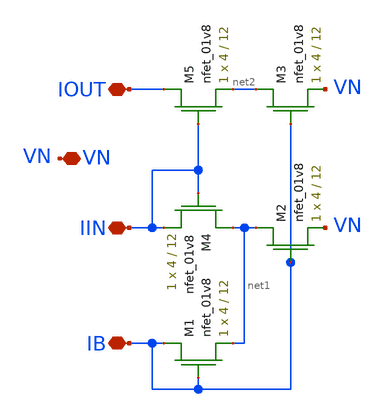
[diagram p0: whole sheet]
** sch_path: dac/layout/current_mirror/lvs_mirror_layout.sch
**.subckt lvs_mirror_layout VN IOUT IIN IB
*.iopin VN
*.iopin IOUT
*.iopin IIN
*.iopin IB
XM1 IB IB net1 VN sky130_fd_pr__nfet_01v8 L=12 W=4 nf=1 ad='int((nf+1)/2) * W/nf * 0.29' as='int((nf+2)/2) * W/nf * 0.29'
+ pd='2*int((nf+1)/2) * (W/nf + 0.29)' ps='2*int((nf+2)/2) * (W/nf + 0.29)' nrd='0.29 / W' nrs='0.29 / W'
+ sa=0 sb=0 sd=0 mult=1 m=1
XM2 net1 IB VN VN sky130_fd_pr__nfet_01v8 L=12 W=4 nf=1 ad='int((nf+1)/2) * W/nf * 0.29' as='int((nf+2)/2) * W/nf * 0.29'
+ pd='2*int((nf+1)/2) * (W/nf + 0.29)' ps='2*int((nf+2)/2) * (W/nf + 0.29)' nrd='0.29 / W' nrs='0.29 / W'
+ sa=0 sb=0 sd=0 mult=1 m=1
XM3 net2 IB VN VN sky130_fd_pr__nfet_01v8 L=12 W=4 nf=1 ad='int((nf+1)/2) * W/nf * 0.29' as='int((nf+2)/2) * W/nf * 0.29'
+ pd='2*int((nf+1)/2) * (W/nf + 0.29)' ps='2*int((nf+2)/2) * (W/nf + 0.29)' nrd='0.29 / W' nrs='0.29 / W'
+ sa=0 sb=0 sd=0 mult=1 m=1
XM4 net1 IIN IIN VN sky130_fd_pr__nfet_01v8 L=12 W=4 nf=1 ad='int((nf+1)/2) * W/nf * 0.29' as='int((nf+2)/2) * W/nf * 0.29'
+ pd='2*int((nf+1)/2) * (W/nf + 0.29)' ps='2*int((nf+2)/2) * (W/nf + 0.29)' nrd='0.29 / W' nrs='0.29 / W'
+ sa=0 sb=0 sd=0 mult=1 m=1
XM5 IOUT IIN net2 VN sky130_fd_pr__nfet_01v8 L=12 W=4 nf=1 ad='int((nf+1)/2) * W/nf * 0.29' as='int((nf+2)/2) * W/nf * 0.29'
+ pd='2*int((nf+1)/2) * (W/nf + 0.29)' ps='2*int((nf+2)/2) * (W/nf + 0.29)' nrd='0.29 / W' nrs='0.29 / W'
+ sa=0 sb=0 sd=0 mult=1 m=1
**.ends
.end
